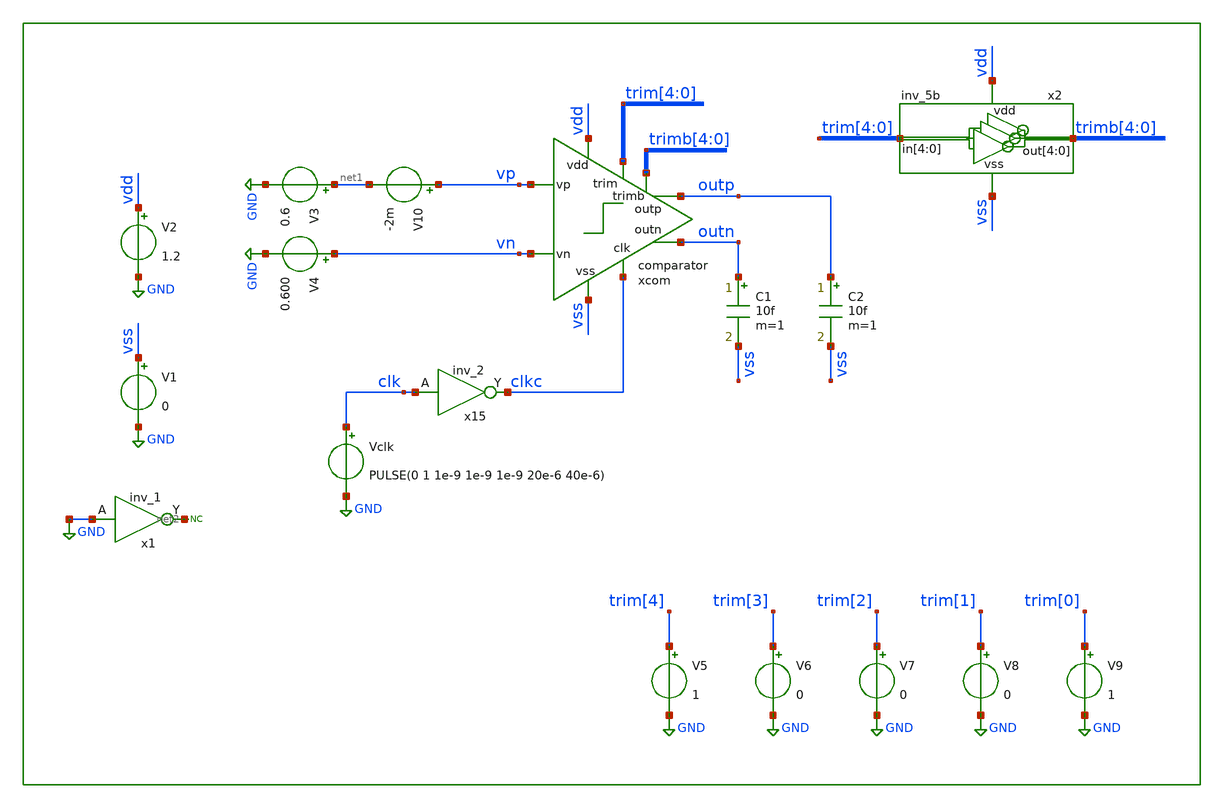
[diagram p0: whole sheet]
** sch_path: xschem/tb/comparator/tran_comparator.sch
**.subckt tran_comparator
xcom vss vdd clkc outp vp outn vn trim[4] trim[3] trim[2] trim[1] trim[0] trimb[4] trimb[3] trimb[2]
+ trimb[1] trimb[0] comparator
x15 clk vss vss vdd vdd clkc sky130_fd_sc_hd__inv_2
V1 vss GND 0
V2 vdd GND 1.2
C1 outn vss 10f m=1
C2 outp vss 10f m=1
Vclk clk GND PULSE(0 1 1e-9 1e-9 1e-9 20e-6 40e-6)
V3 net1 GND 0.6
V4 vn GND 0.600
* noconn #net2
V5 trim[4] GND 1
V6 trim[3] GND 0
V7 trim[2] GND 0
V8 trim[1] GND 0
V9 trim[0] GND 1
x1 GND vss vss vdd vdd net2 sky130_fd_sc_hd__inv_1
x2 vdd trimb[4] trimb[3] trimb[2] trimb[1] trimb[0] trim[4] trim[3] trim[2] trim[1] trim[0] vss
+ inv_5b
V10 vp net1 -2m
**** begin user architecture code
[sky130_models]

*.include $::DESIGN_PATH/design/tb/comparator/ctl.sp

*vt0 trim_0_ 0 1.2
*vt1 trim_1_ 0 1.2
*vt2 trim_2_ 0 1.2
*vt3 trim_3_ 0 1.2
*vt4 trim_4_ 0 1.2

.options method trap

.control
.param MC_SWITCH=0

tran 100e-9 100e-6
plt outp
.endc


* FET CORNERS
.include $::SKYWATER_MODELS/corners/tt.spice
*.include $::SKYWATER_MODELS/corners/ff.spice
*.include $::SKYWATER_MODELS/corners/ss.spice
*.include $::SKYWATER_MODELS/corners/sf.spice
*.include $::SKYWATER_MODELS/corners/fs.spice

* TT + R + C
*.include $::SKYWATER_MODELS/corners/tt_rmax_cmax.spice
*.include $::SKYWATER_MODELS/corners/tt_rmin_cmin.spice
*.include $::SKYWATER_MODELS/corners/tt_rmax_cmin.spice
*.include $::SKYWATER_MODELS/corners/tt_rmin_cmax.spice

* FF + R + C
*.include $::SKYWATER_MODELS/corners/ff_rmax_cmax.spice
*.include $::SKYWATER_MODELS/corners/ff_rmin_cmin.spice
*.include $::SKYWATER_MODELS/corners/ff_rmax_cmin.spice
*.include $::SKYWATER_MODELS/corners/ff_rmin_cmax.spice


* SS + R + C
*.include $::SKYWATER_MODELS/corners/ss_rmax_cmax.spice
*.include $::SKYWATER_MODELS/corners/ss_rmin_cmin.spice
*.include $::SKYWATER_MODELS/corners/ss_rmax_cmin.spice
*.include $::SKYWATER_MODELS/corners/ss_rmin_cmax.spice

* SF + R + C
*.include $::SKYWATER_MODELS/corners/sf_rmax_cmax.spice
*.include $::SKYWATER_MODELS/corners/sf_rmin_cmin.spice
*.include $::SKYWATER_MODELS/corners/sf_rmax_cmin.spice
*.include $::SKYWATER_MODELS/corners/sf_rmin_cmax.spice

* FS + R + C
*.include $::SKYWATER_MODELS/corners/fs_rmax_cmax.spice
*.include $::SKYWATER_MODELS/corners/fs_rmin_cmin.spice
*.include $::SKYWATER_MODELS/corners/fs_rmax_cmin.spice
*.include $::SKYWATER_MODELS/corners/fs_rmin_cmax.spice

**** end user architecture code
**.ends

* expanding   symbol:  sar_10b/comparator/comparator.sym # of pins=9
** sym_path: xschem/sar_10b/comparator/comparator.sym
** sch_path: xschem/sar_10b/comparator/comparator.sch
.subckt comparator vss vdd clk outp vp outn vn trim[4] trim[3] trim[2] trim[1] trim[0] trimb[4]
+ trimb[3] trimb[2] trimb[1] trimb[0]
*.ipin vn
*.ipin vp
*.ipin clk
*.iopin vdd
*.iopin vss
*.opin outp
*.opin outn
*.ipin trim[4],trim[3],trim[2],trim[1],trim[0]
*.ipin trimb[4],trimb[3],trimb[2],trimb[1],trimb[0]
XMdiff diff clk vss vss sky130_fd_pr__nfet_01v8 L=0.3 W=1 nf=1 ad='int((nf+1)/2) * W/nf * 0.29' as='int((nf+2)/2) * W/nf * 0.29'
+ pd='2*int((nf+1)/2) * (W/nf + 0.29)' ps='2*int((nf+2)/2) * (W/nf + 0.29)' nrd='0.29 / W' nrs='0.29 / W'
+ sa=0 sb=0 sd=0 mult=2 m=2
XMinn in vn diff vss sky130_fd_pr__nfet_01v8 L=0.3 W=1 nf=1 ad='int((nf+1)/2) * W/nf * 0.29' as='int((nf+2)/2) * W/nf * 0.29'
+ pd='2*int((nf+1)/2) * (W/nf + 0.29)' ps='2*int((nf+2)/2) * (W/nf + 0.29)' nrd='0.29 / W' nrs='0.29 / W'
+ sa=0 sb=0 sd=0 mult=1 m=1
XMinp ip vp diff vss sky130_fd_pr__nfet_01v8 L=0.3 W=1 nf=1 ad='int((nf+1)/2) * W/nf * 0.29' as='int((nf+2)/2) * W/nf * 0.29'
+ pd='2*int((nf+1)/2) * (W/nf + 0.29)' ps='2*int((nf+2)/2) * (W/nf + 0.29)' nrd='0.29 / W' nrs='0.29 / W'
+ sa=0 sb=0 sd=0 mult=1 m=1
XMl4 outp outn vdd vdd sky130_fd_pr__pfet_01v8 L=0.3 W=1 nf=1 ad='int((nf+1)/2) * W/nf * 0.29' as='int((nf+2)/2) * W/nf * 0.29'
+ pd='2*int((nf+1)/2) * (W/nf + 0.29)' ps='2*int((nf+2)/2) * (W/nf + 0.29)' nrd='0.29 / W' nrs='0.29 / W'
+ sa=0 sb=0 sd=0 mult=1 m=1
XMl3 outn outp vdd vdd sky130_fd_pr__pfet_01v8 L=0.3 W=1 nf=1 ad='int((nf+1)/2) * W/nf * 0.29' as='int((nf+2)/2) * W/nf * 0.29'
+ pd='2*int((nf+1)/2) * (W/nf + 0.29)' ps='2*int((nf+2)/2) * (W/nf + 0.29)' nrd='0.29 / W' nrs='0.29 / W'
+ sa=0 sb=0 sd=0 mult=1 m=1
XM3 outp clk vdd vdd sky130_fd_pr__pfet_01v8 L=0.3 W=1 nf=1 ad='int((nf+1)/2) * W/nf * 0.29' as='int((nf+2)/2) * W/nf * 0.29'
+ pd='2*int((nf+1)/2) * (W/nf + 0.29)' ps='2*int((nf+2)/2) * (W/nf + 0.29)' nrd='0.29 / W' nrs='0.29 / W'
+ sa=0 sb=0 sd=0 mult=1 m=1
XM2 outn clk vdd vdd sky130_fd_pr__pfet_01v8 L=0.3 W=1 nf=1 ad='int((nf+1)/2) * W/nf * 0.29' as='int((nf+2)/2) * W/nf * 0.29'
+ pd='2*int((nf+1)/2) * (W/nf + 0.29)' ps='2*int((nf+2)/2) * (W/nf + 0.29)' nrd='0.29 / W' nrs='0.29 / W'
+ sa=0 sb=0 sd=0 mult=1 m=1
XMl1 outn outp in vss sky130_fd_pr__nfet_01v8 L=0.3 W=1 nf=1 ad='int((nf+1)/2) * W/nf * 0.29' as='int((nf+2)/2) * W/nf * 0.29'
+ pd='2*int((nf+1)/2) * (W/nf + 0.29)' ps='2*int((nf+2)/2) * (W/nf + 0.29)' nrd='0.29 / W' nrs='0.29 / W'
+ sa=0 sb=0 sd=0 mult=1 m=1
XMl2 outp outn ip vss sky130_fd_pr__nfet_01v8 L=0.3 W=1 nf=1 ad='int((nf+1)/2) * W/nf * 0.29' as='int((nf+2)/2) * W/nf * 0.29'
+ pd='2*int((nf+1)/2) * (W/nf + 0.29)' ps='2*int((nf+2)/2) * (W/nf + 0.29)' nrd='0.29 / W' nrs='0.29 / W'
+ sa=0 sb=0 sd=0 mult=1 m=1
XM4 ip clk vdd vdd sky130_fd_pr__pfet_01v8 L=0.3 W=1 nf=1 ad='int((nf+1)/2) * W/nf * 0.29' as='int((nf+2)/2) * W/nf * 0.29'
+ pd='2*int((nf+1)/2) * (W/nf + 0.29)' ps='2*int((nf+2)/2) * (W/nf + 0.29)' nrd='0.29 / W' nrs='0.29 / W'
+ sa=0 sb=0 sd=0 mult=1 m=1
XM1 in clk vdd vdd sky130_fd_pr__pfet_01v8 L=0.3 W=1 nf=1 ad='int((nf+1)/2) * W/nf * 0.29' as='int((nf+2)/2) * W/nf * 0.29'
+ pd='2*int((nf+1)/2) * (W/nf + 0.29)' ps='2*int((nf+2)/2) * (W/nf + 0.29)' nrd='0.29 / W' nrs='0.29 / W'
+ sa=0 sb=0 sd=0 mult=1 m=1
x2 in trim[4] trim[3] trim[2] trim[1] trim[0] vss trim
x3 ip trimb[4] trimb[3] trimb[2] trimb[1] trimb[0] vss trim
.ends


* expanding   symbol:  support/inv_5b.sym # of pins=4
** sym_path: xschem/support/inv_5b.sym
** sch_path: xschem/support/inv_5b.sch
.subckt inv_5b vdd out[4] out[3] out[2] out[1] out[0] in[4] in[3] in[2] in[1] in[0] vss
*.opin out[4],out[3],out[2],out[1],out[0]
*.iopin vdd
*.iopin vss
*.ipin in[4],in[3],in[2],in[1],in[0]
x0 in[0] vss vss vdd vdd out[0] sky130_fd_sc_hd__inv_1
x1 in[1] vss vss vdd vdd out[1] sky130_fd_sc_hd__inv_1
x2 in[2] vss vss vdd vdd out[2] sky130_fd_sc_hd__inv_1
x3 in[3] vss vss vdd vdd out[3] sky130_fd_sc_hd__inv_1
x4 in[4] vss vss vdd vdd out[4] sky130_fd_sc_hd__inv_1
.ends


* expanding   symbol:  sar_10b/comparator/trim.sym # of pins=3
** sym_path: xschem/sar_10b/comparator/trim.sym
** sch_path: xschem/sar_10b/comparator/trim.sch
.subckt trim drain d[4] d[3] d[2] d[1] d[0] vss
*.iopin vss
*.ipin d[4],d[3],d[2],d[1],d[0]
*.opin drain
XM4[7] n4 d[4] vss vss sky130_fd_pr__nfet_01v8_lvt L=0.3 W=1 nf=1 ad='int((nf+1)/2) * W/nf * 0.29' as='int((nf+2)/2) * W/nf * 0.29'
+ pd='2*int((nf+1)/2) * (W/nf + 0.29)' ps='2*int((nf+2)/2) * (W/nf + 0.29)' nrd='0.29 / W' nrs='0.29 / W'
+ sa=0 sb=0 sd=0 mult=1 m=1
XM4[6] n4 d[4] vss vss sky130_fd_pr__nfet_01v8_lvt L=0.3 W=1 nf=1 ad='int((nf+1)/2) * W/nf * 0.29' as='int((nf+2)/2) * W/nf * 0.29'
+ pd='2*int((nf+1)/2) * (W/nf + 0.29)' ps='2*int((nf+2)/2) * (W/nf + 0.29)' nrd='0.29 / W' nrs='0.29 / W'
+ sa=0 sb=0 sd=0 mult=1 m=1
XM4[5] n4 d[4] vss vss sky130_fd_pr__nfet_01v8_lvt L=0.3 W=1 nf=1 ad='int((nf+1)/2) * W/nf * 0.29' as='int((nf+2)/2) * W/nf * 0.29'
+ pd='2*int((nf+1)/2) * (W/nf + 0.29)' ps='2*int((nf+2)/2) * (W/nf + 0.29)' nrd='0.29 / W' nrs='0.29 / W'
+ sa=0 sb=0 sd=0 mult=1 m=1
XM4[4] n4 d[4] vss vss sky130_fd_pr__nfet_01v8_lvt L=0.3 W=1 nf=1 ad='int((nf+1)/2) * W/nf * 0.29' as='int((nf+2)/2) * W/nf * 0.29'
+ pd='2*int((nf+1)/2) * (W/nf + 0.29)' ps='2*int((nf+2)/2) * (W/nf + 0.29)' nrd='0.29 / W' nrs='0.29 / W'
+ sa=0 sb=0 sd=0 mult=1 m=1
XM4[3] n4 d[4] vss vss sky130_fd_pr__nfet_01v8_lvt L=0.3 W=1 nf=1 ad='int((nf+1)/2) * W/nf * 0.29' as='int((nf+2)/2) * W/nf * 0.29'
+ pd='2*int((nf+1)/2) * (W/nf + 0.29)' ps='2*int((nf+2)/2) * (W/nf + 0.29)' nrd='0.29 / W' nrs='0.29 / W'
+ sa=0 sb=0 sd=0 mult=1 m=1
XM4[2] n4 d[4] vss vss sky130_fd_pr__nfet_01v8_lvt L=0.3 W=1 nf=1 ad='int((nf+1)/2) * W/nf * 0.29' as='int((nf+2)/2) * W/nf * 0.29'
+ pd='2*int((nf+1)/2) * (W/nf + 0.29)' ps='2*int((nf+2)/2) * (W/nf + 0.29)' nrd='0.29 / W' nrs='0.29 / W'
+ sa=0 sb=0 sd=0 mult=1 m=1
XM4[1] n4 d[4] vss vss sky130_fd_pr__nfet_01v8_lvt L=0.3 W=1 nf=1 ad='int((nf+1)/2) * W/nf * 0.29' as='int((nf+2)/2) * W/nf * 0.29'
+ pd='2*int((nf+1)/2) * (W/nf + 0.29)' ps='2*int((nf+2)/2) * (W/nf + 0.29)' nrd='0.29 / W' nrs='0.29 / W'
+ sa=0 sb=0 sd=0 mult=1 m=1
XM4[0] n4 d[4] vss vss sky130_fd_pr__nfet_01v8_lvt L=0.3 W=1 nf=1 ad='int((nf+1)/2) * W/nf * 0.29' as='int((nf+2)/2) * W/nf * 0.29'
+ pd='2*int((nf+1)/2) * (W/nf + 0.29)' ps='2*int((nf+2)/2) * (W/nf + 0.29)' nrd='0.29 / W' nrs='0.29 / W'
+ sa=0 sb=0 sd=0 mult=1 m=1
XM3[3] n3 d[3] vss vss sky130_fd_pr__nfet_01v8_lvt L=0.3 W=1 nf=1 ad='int((nf+1)/2) * W/nf * 0.29' as='int((nf+2)/2) * W/nf * 0.29'
+ pd='2*int((nf+1)/2) * (W/nf + 0.29)' ps='2*int((nf+2)/2) * (W/nf + 0.29)' nrd='0.29 / W' nrs='0.29 / W'
+ sa=0 sb=0 sd=0 mult=1 m=1
XM3[2] n3 d[3] vss vss sky130_fd_pr__nfet_01v8_lvt L=0.3 W=1 nf=1 ad='int((nf+1)/2) * W/nf * 0.29' as='int((nf+2)/2) * W/nf * 0.29'
+ pd='2*int((nf+1)/2) * (W/nf + 0.29)' ps='2*int((nf+2)/2) * (W/nf + 0.29)' nrd='0.29 / W' nrs='0.29 / W'
+ sa=0 sb=0 sd=0 mult=1 m=1
XM3[1] n3 d[3] vss vss sky130_fd_pr__nfet_01v8_lvt L=0.3 W=1 nf=1 ad='int((nf+1)/2) * W/nf * 0.29' as='int((nf+2)/2) * W/nf * 0.29'
+ pd='2*int((nf+1)/2) * (W/nf + 0.29)' ps='2*int((nf+2)/2) * (W/nf + 0.29)' nrd='0.29 / W' nrs='0.29 / W'
+ sa=0 sb=0 sd=0 mult=1 m=1
XM3[0] n3 d[3] vss vss sky130_fd_pr__nfet_01v8_lvt L=0.3 W=1 nf=1 ad='int((nf+1)/2) * W/nf * 0.29' as='int((nf+2)/2) * W/nf * 0.29'
+ pd='2*int((nf+1)/2) * (W/nf + 0.29)' ps='2*int((nf+2)/2) * (W/nf + 0.29)' nrd='0.29 / W' nrs='0.29 / W'
+ sa=0 sb=0 sd=0 mult=1 m=1
XM2[1] n2 d[2] vss vss sky130_fd_pr__nfet_01v8_lvt L=0.3 W=1 nf=1 ad='int((nf+1)/2) * W/nf * 0.29' as='int((nf+2)/2) * W/nf * 0.29'
+ pd='2*int((nf+1)/2) * (W/nf + 0.29)' ps='2*int((nf+2)/2) * (W/nf + 0.29)' nrd='0.29 / W' nrs='0.29 / W'
+ sa=0 sb=0 sd=0 mult=1 m=1
XM2[0] n2 d[2] vss vss sky130_fd_pr__nfet_01v8_lvt L=0.3 W=1 nf=1 ad='int((nf+1)/2) * W/nf * 0.29' as='int((nf+2)/2) * W/nf * 0.29'
+ pd='2*int((nf+1)/2) * (W/nf + 0.29)' ps='2*int((nf+2)/2) * (W/nf + 0.29)' nrd='0.29 / W' nrs='0.29 / W'
+ sa=0 sb=0 sd=0 mult=1 m=1
XM1 n1 d[1] vss vss sky130_fd_pr__nfet_01v8_lvt L=0.3 W=1 nf=1 ad='int((nf+1)/2) * W/nf * 0.29' as='int((nf+2)/2) * W/nf * 0.29'
+ pd='2*int((nf+1)/2) * (W/nf + 0.29)' ps='2*int((nf+2)/2) * (W/nf + 0.29)' nrd='0.29 / W' nrs='0.29 / W'
+ sa=0 sb=0 sd=0 mult=1 m=1
XM0 n0 d[0] vss vss sky130_fd_pr__nfet_01v8_lvt L=0.3 W=1 nf=1 ad='int((nf+1)/2) * W/nf * 0.29' as='int((nf+2)/2) * W/nf * 0.29'
+ pd='2*int((nf+1)/2) * (W/nf + 0.29)' ps='2*int((nf+2)/2) * (W/nf + 0.29)' nrd='0.29 / W' nrs='0.29 / W'
+ sa=0 sb=0 sd=0 mult=1 m=1
x4[7] drain n4 trimcap
x4[6] drain n4 trimcap
x4[5] drain n4 trimcap
x4[4] drain n4 trimcap
x4[3] drain n4 trimcap
x4[2] drain n4 trimcap
x4[1] drain n4 trimcap
x4[0] drain n4 trimcap
x3[3] drain n3 trimcap
x3[2] drain n3 trimcap
x3[1] drain n3 trimcap
x3[0] drain n3 trimcap
x2[1] drain n2 trimcap
x2[0] drain n2 trimcap
x1 drain n1 trimcap
x0 drain n0 trimcap
.ends


* expanding   symbol:  sar_10b/comparator/trimcap.sym # of pins=2
** sym_path: xschem/sar_10b/comparator/trimcap.sym
** sch_path: xschem/sar_10b/comparator/trimcap.sch
.subckt trimcap cp cn
*.iopin cp
*.iopin cn
c0 net1 cn 2f m=1
c1 cp net1 1f m=1
.ends

.GLOBAL GND
.end
